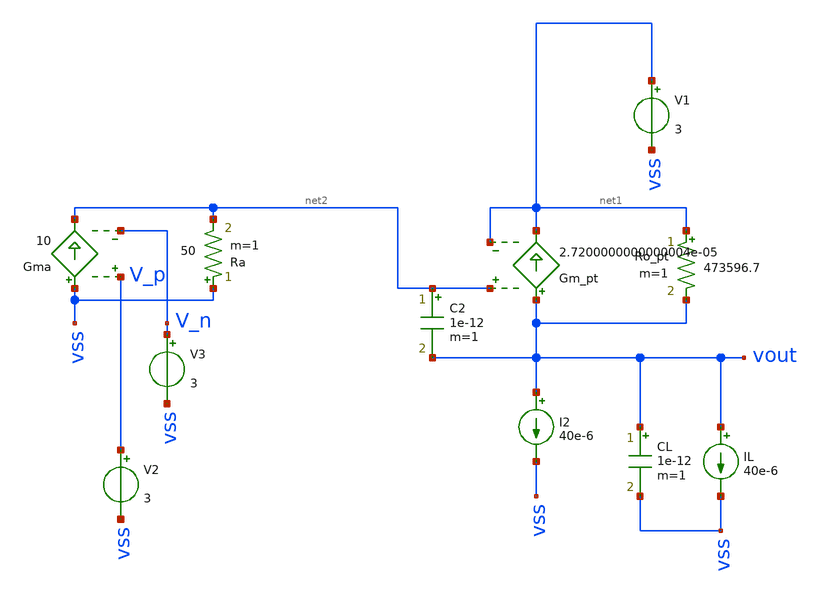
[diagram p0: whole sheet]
** sch_path: test/sstadex/xschem/stage2_OTA.sch
**.subckt stage2_OTA
Ro_pt net1 vout 473596.7 m=1
Gm_pt vout net1 net2 net1 2.7200000000000004e-05
Gma vss net2 V_p V_n 10
Ra vss net2 50 m=1
V1 net1 vss 3
V3 V_n vss 3
I2 vout vss 40e-6
V2 V_p vss 3
CL vout vss 1e-12 m=1
C2 net2 vout 1e-12 m=1
IL vout vss 40e-6
**.ends
.end
